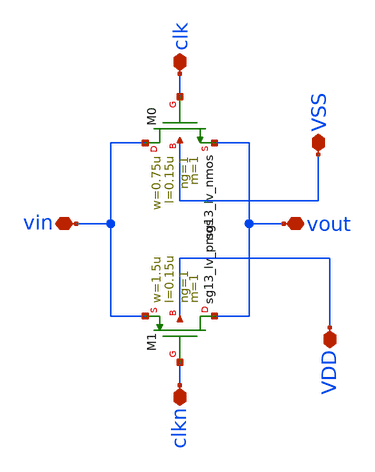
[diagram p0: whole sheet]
** sch_path: design/blocks/transmissiongate/schematic/transmissiongate.sch
**.subckt transmissiongate vout vin clk clkn VSS VDD
*.iopin vout
*.iopin vin
*.iopin clk
*.iopin clkn
*.iopin VSS
*.iopin VDD
XM1 vout clkn vin VDD sg13_lv_pmos w=1.5u l=0.15u ng=1 m=1 mm_ok=1
XM0 vin clk vout VSS sg13_lv_nmos w=0.75u l=0.15u ng=1 m=1 mm_ok=1
**.ends
.end
